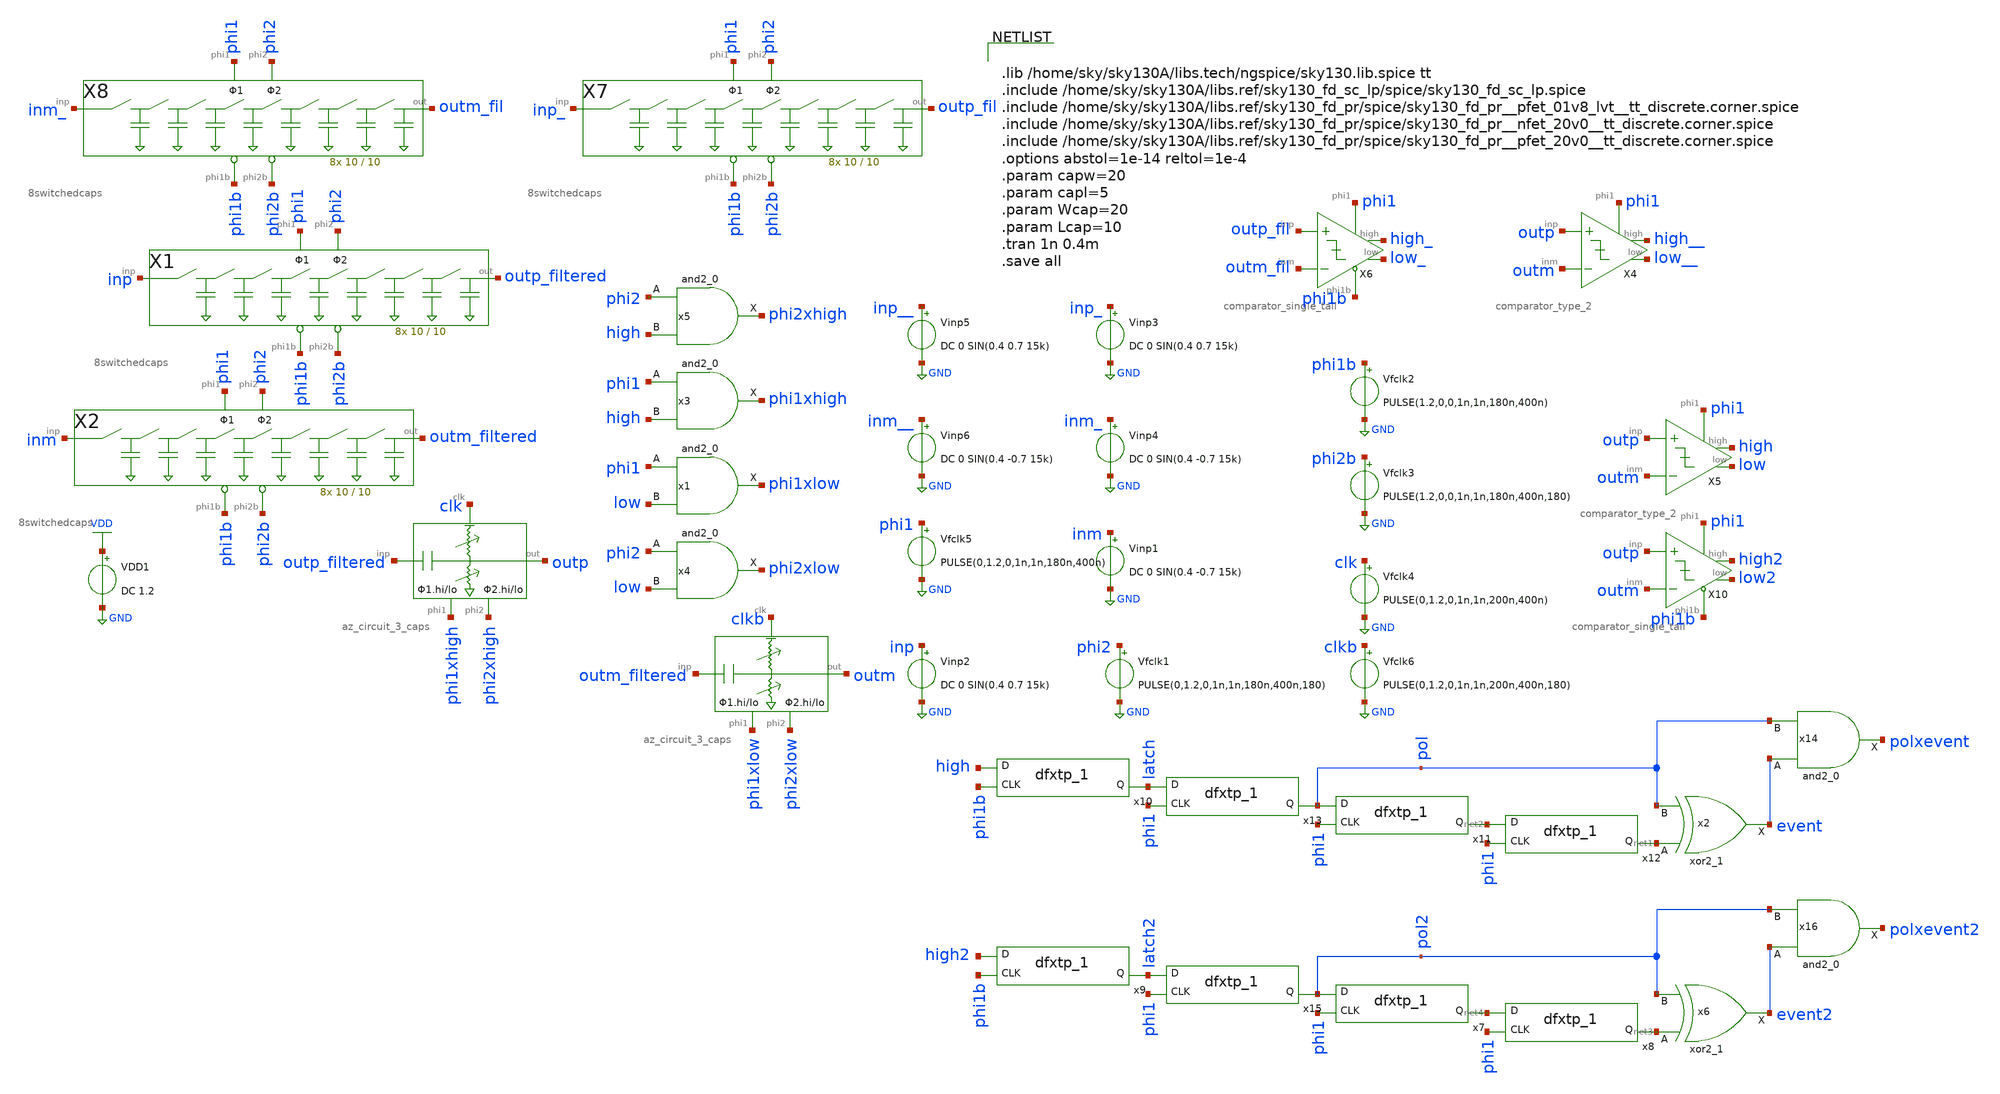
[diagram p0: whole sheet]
** sch_path: xschem/archive/comparator_latest/gauss_comp.sch
**.subckt gauss_comp
VDD1 VDD GND DC 1.2
Vfclk5 phi1 GND PULSE(0,1.2,0,1n,1n,180n,400n)
Vfclk1 phi2 GND PULSE(0,1.2,0,1n,1n,180n,400n,180)
Vfclk2 phi1b GND PULSE(1.2,0,0,1n,1n,180n,400n)
Vfclk3 phi2b GND PULSE(1.2,0,0,1n,1n,180n,400n,180)
Vinp2 inp GND DC 0 SIN(0.4 0.7 15k)
Vinp1 inm GND DC 0 SIN(0.4 -0.7 15k)
x1 phi1 low GND GND VDD VDD phi1xlow sky130_fd_sc_lp__and2_0
x3 phi1 high GND GND VDD VDD phi1xhigh sky130_fd_sc_lp__and2_0
x4 phi2 low GND GND VDD VDD phi2xlow sky130_fd_sc_lp__and2_0
x5 phi2 high GND GND VDD VDD phi2xhigh sky130_fd_sc_lp__and2_0
Vfclk4 clk GND PULSE(0,1.2,0,1n,1n,200n,400n)
Vfclk6 clkb GND PULSE(0,1.2,0,1n,1n,200n,400n,180)
X1 inp outp_filtered phi2 phi1 phi1b phi2b 8switchedcaps Wcap=10 Lcap=10
X2 inm outm_filtered phi2 phi1 phi1b phi2b 8switchedcaps Wcap=10 Lcap=10
X6 outp_fil outm_fil high_ phi1 phi1b low_ comparator_single_tail Wplus=1.75 Lplus=1.75 Wminus=1.75
+ Lminus=0.15
X7 inp_ outp_fil phi2 phi1 phi1b phi2b 8switchedcaps Wcap=10 Lcap=10
X8 inm_ outm_fil phi2 phi1 phi1b phi2b 8switchedcaps Wcap=10 Lcap=10
Vinp3 inp_ GND DC 0 SIN(0.4 0.7 15k)
Vinp4 inm_ GND DC 0 SIN(0.4 -0.7 15k)
Vinp5 inp__ GND DC 0 SIN(0.4 0.7 15k)
Vinp6 inm__ GND DC 0 SIN(0.4 -0.7 15k)
X3 outp_filtered outp phi1xhigh phi2xhigh clk az_circuit_3_caps Wcap=10 Lcap=10
X9 outm_filtered outm phi1xlow phi2xlow clkb az_circuit_3_caps Wcap=10 Lcap=10
x2 net1 pol GND GND VDD VDD event sky130_fd_sc_lp__xor2_1
x11 phi1 pol gnd gnd vdd vdd net2 sky130_fd_sc_lp__dfxtp_1
x12 phi1 net2 gnd gnd vdd vdd net1 sky130_fd_sc_lp__dfxtp_1
x10 phi1b high gnd gnd vdd vdd latch sky130_fd_sc_lp__dfxtp_1
x13 phi1 latch gnd gnd vdd vdd pol sky130_fd_sc_lp__dfxtp_1
x14 event pol GND GND VDD VDD polxevent sky130_fd_sc_lp__and2_0
x6 net3 pol2 GND GND VDD VDD event2 sky130_fd_sc_lp__xor2_1
x7 phi1 pol2 gnd gnd vdd vdd net4 sky130_fd_sc_lp__dfxtp_1
x8 phi1 net4 gnd gnd vdd vdd net3 sky130_fd_sc_lp__dfxtp_1
x9 phi1b high2 gnd gnd vdd vdd latch2 sky130_fd_sc_lp__dfxtp_1
x15 phi1 latch2 gnd gnd vdd vdd pol2 sky130_fd_sc_lp__dfxtp_1
x16 event2 pol2 GND GND VDD VDD polxevent2 sky130_fd_sc_lp__and2_0
X4 outp outm high__ phi1 low__ comparator_type_2 Wplus=0.42 Lplus=0.42 Wminus=0.42 Lminus=0.15
X5 outp outm high phi1 low comparator_type_2 Wplus=0.42 Lplus=0.42 Wminus=0.42 Lminus=0.15
X10 outp outm high2 phi1 phi1b low2 comparator_single_tail Wplus=1.75 Lplus=1.75 Wminus=1.75
+ Lminus=0.15
**** begin user architecture code


.lib /home/sky/sky130A/libs.tech/ngspice/sky130.lib.spice tt
.include /home/sky/sky130A/libs.ref/sky130_fd_sc_lp/spice/sky130_fd_sc_lp.spice
.include /home/sky/sky130A/libs.ref/sky130_fd_pr/spice/sky130_fd_pr__pfet_01v8_lvt__tt_discrete.corner.spice
.include /home/sky/sky130A/libs.ref/sky130_fd_pr/spice/sky130_fd_pr__nfet_20v0__tt_discrete.corner.spice
.include /home/sky/sky130A/libs.ref/sky130_fd_pr/spice/sky130_fd_pr__pfet_20v0__tt_discrete.corner.spice
.options abstol=1e-14 reltol=1e-4
.param capw=20
.param capl=5
.param Wcap=20
.param Lcap=10
.tran 1n 0.4m
.save all


**** end user architecture code
**.ends
.GLOBAL GND
.GLOBAL VDD
.end
